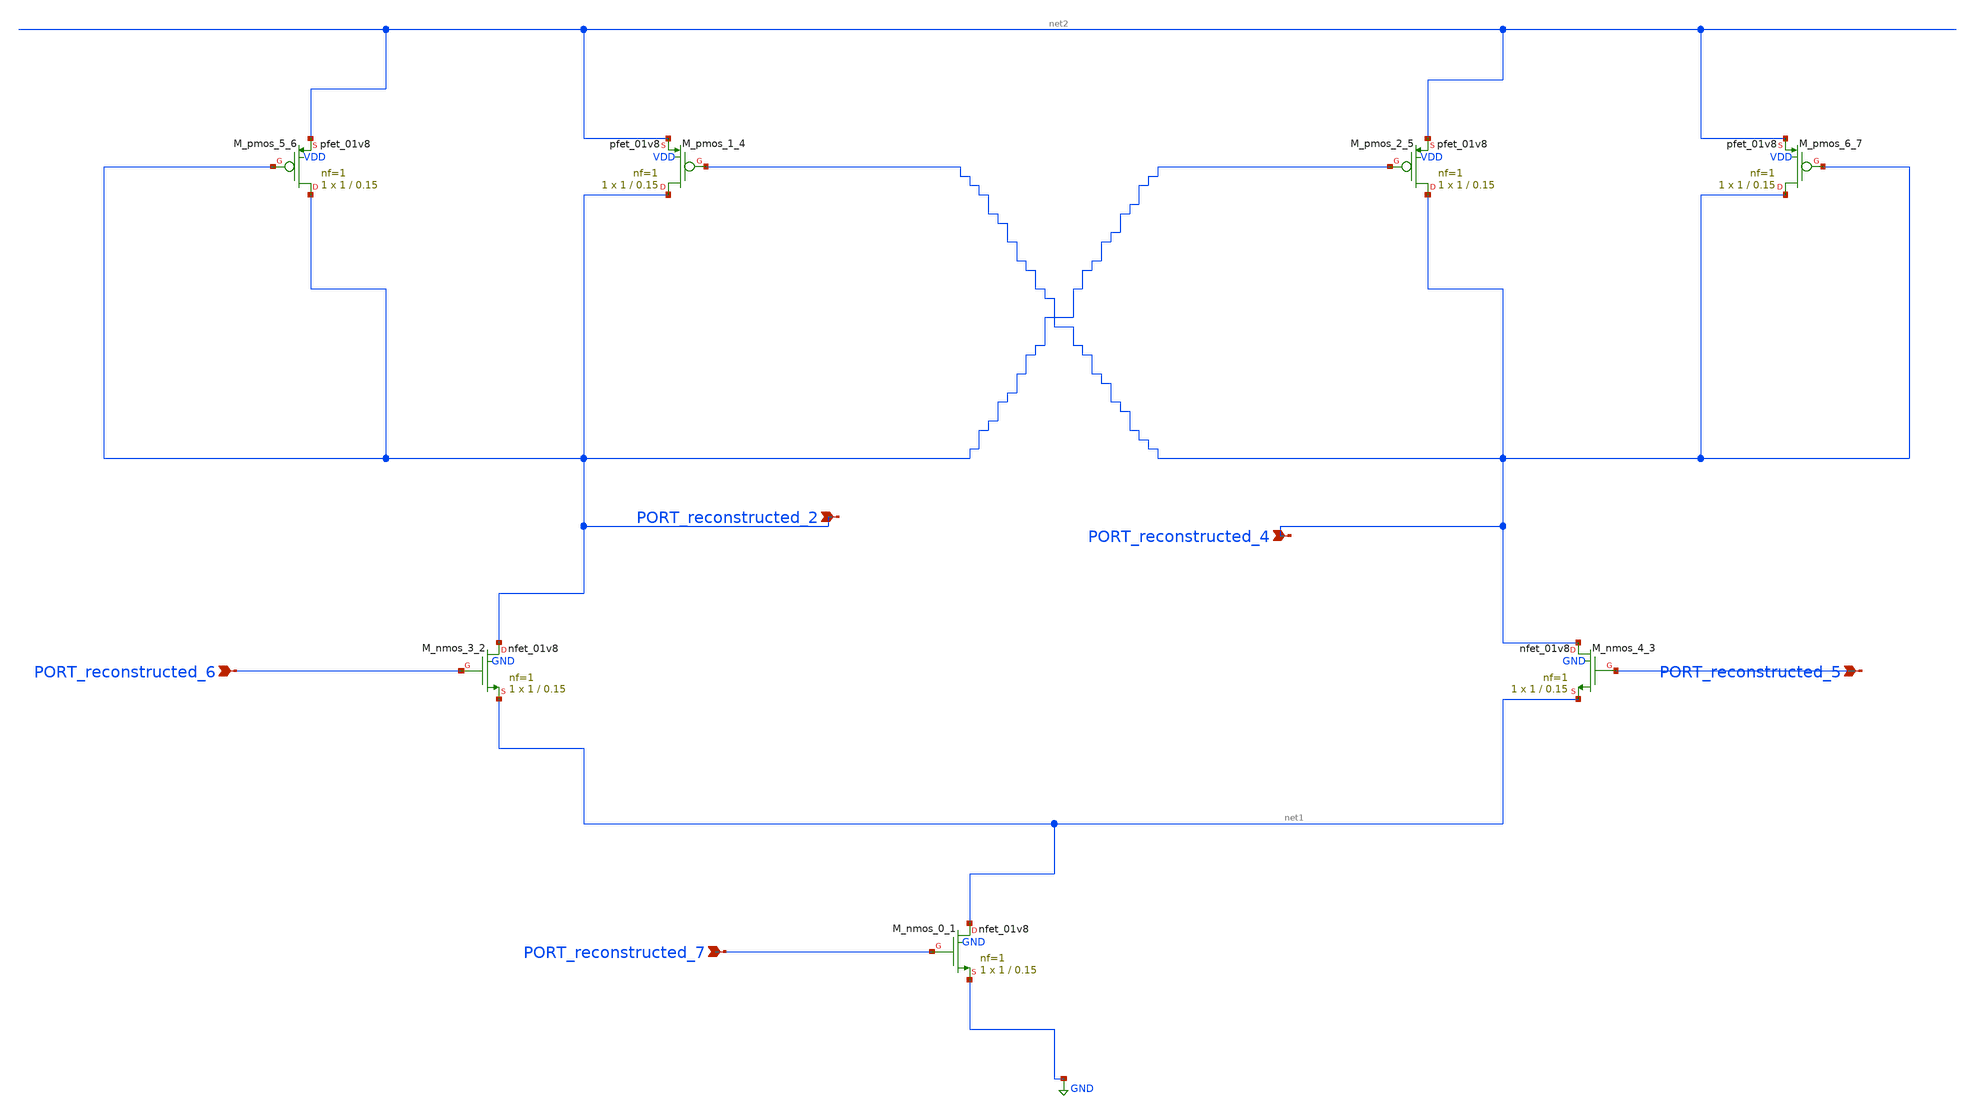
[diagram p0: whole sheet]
** sch_path: schematics/AMSNet/245.sch
**.subckt 245 PORT_reconstructed_5 PORT_reconstructed_4 PORT_reconstructed_6 PORT_reconstructed_7
*+ PORT_reconstructed_2
*.ipin PORT_reconstructed_5
*.ipin PORT_reconstructed_4
*.ipin PORT_reconstructed_6
*.ipin PORT_reconstructed_7
*.ipin PORT_reconstructed_2
XM_nmos_0_1 net1 PORT_reconstructed_7 GND GND sky130_fd_pr__nfet_01v8 L=0.15 W=1 nf=1 ad='int((1 + 1)/2) * 1 / 1 * 0.29'
+ as='int((1 + 2)/2) * 1 / 1 * 0.29' pd='2*int((1 + 1)/2) * (1 / 1 + 0.29)' ps='2*int((1 + 2)/2) * (1 / 1 + 0.29)'
+ nrd='0.29 / 1 ' nrs='0.29 / 1 ' sa=0 sb=0 sd=0 mult=1 m=1
XM_nmos_3_2 PORT_reconstructed_2 PORT_reconstructed_6 net1 GND sky130_fd_pr__nfet_01v8 L=0.15 W=1 nf=1
+ ad='int((1 + 1)/2) * 1 / 1 * 0.29' as='int((1 + 2)/2) * 1 / 1 * 0.29' pd='2*int((1 + 1)/2) * (1 / 1 + 0.29)'
+ ps='2*int((1 + 2)/2) * (1 / 1 + 0.29)' nrd='0.29 / 1 ' nrs='0.29 / 1 ' sa=0 sb=0 sd=0 mult=1 m=1
XM_nmos_4_3 PORT_reconstructed_4 PORT_reconstructed_5 net1 GND sky130_fd_pr__nfet_01v8 L=0.15 W=1 nf=1
+ ad='int((1 + 1)/2) * 1 / 1 * 0.29' as='int((1 + 2)/2) * 1 / 1 * 0.29' pd='2*int((1 + 1)/2) * (1 / 1 + 0.29)'
+ ps='2*int((1 + 2)/2) * (1 / 1 + 0.29)' nrd='0.29 / 1 ' nrs='0.29 / 1 ' sa=0 sb=0 sd=0 mult=1 m=1
XM_pmos_1_4 PORT_reconstructed_2 PORT_reconstructed_4 net2 VDD sky130_fd_pr__pfet_01v8 L=0.15 W=1 nf=1
+ ad='int((1 + 1)/2) * 1 / 1 * 0.29' as='int((1 + 2)/2) * 1 / 1 * 0.29' pd='2*int((1 + 1)/2) * (1 / 1 + 0.29)'
+ ps='2*int((1 + 2)/2) * (1 / 1 + 0.29)' nrd='0.29 / 1 ' nrs='0.29 / 1 ' sa=0 sb=0 sd=0 mult=1 m=1
XM_pmos_2_5 PORT_reconstructed_4 PORT_reconstructed_2 net2 VDD sky130_fd_pr__pfet_01v8 L=0.15 W=1 nf=1
+ ad='int((1 + 1)/2) * 1 / 1 * 0.29' as='int((1 + 2)/2) * 1 / 1 * 0.29' pd='2*int((1 + 1)/2) * (1 / 1 + 0.29)'
+ ps='2*int((1 + 2)/2) * (1 / 1 + 0.29)' nrd='0.29 / 1 ' nrs='0.29 / 1 ' sa=0 sb=0 sd=0 mult=1 m=1
XM_pmos_5_6 PORT_reconstructed_2 PORT_reconstructed_2 net2 VDD sky130_fd_pr__pfet_01v8 L=0.15 W=1 nf=1
+ ad='int((1 + 1)/2) * 1 / 1 * 0.29' as='int((1 + 2)/2) * 1 / 1 * 0.29' pd='2*int((1 + 1)/2) * (1 / 1 + 0.29)'
+ ps='2*int((1 + 2)/2) * (1 / 1 + 0.29)' nrd='0.29 / 1 ' nrs='0.29 / 1 ' sa=0 sb=0 sd=0 mult=1 m=1
XM_pmos_6_7 PORT_reconstructed_4 PORT_reconstructed_4 net2 VDD sky130_fd_pr__pfet_01v8 L=0.15 W=1 nf=1
+ ad='int((1 + 1)/2) * 1 / 1 * 0.29' as='int((1 + 2)/2) * 1 / 1 * 0.29' pd='2*int((1 + 1)/2) * (1 / 1 + 0.29)'
+ ps='2*int((1 + 2)/2) * (1 / 1 + 0.29)' nrd='0.29 / 1 ' nrs='0.29 / 1 ' sa=0 sb=0 sd=0 mult=1 m=1
**.ends
.GLOBAL GND
.end
